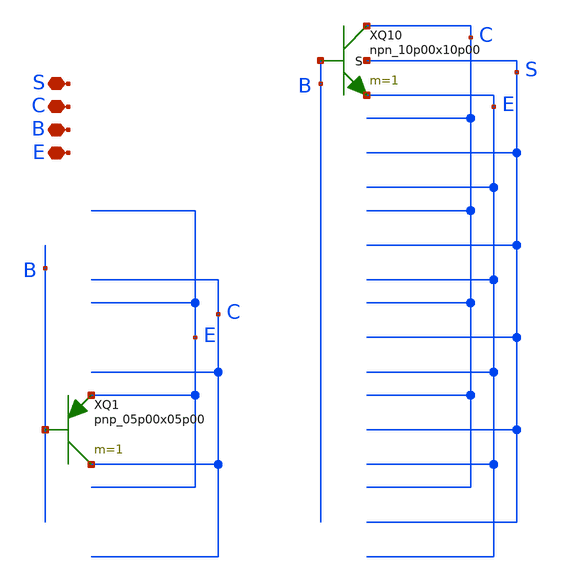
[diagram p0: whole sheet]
** sch_path: samples/gf180mcu/bjt_fast/symbol/bjt_fast.sch
**.subckt bjt_fast C E B S
*.iopin C
*.iopin E
*.iopin B
*.iopin S
XQ1 C B E pnp_05p00x05p00 m=1 par=1
XQ10 C B E S npn_10p00x10p00 m=1
**.ends
.end
